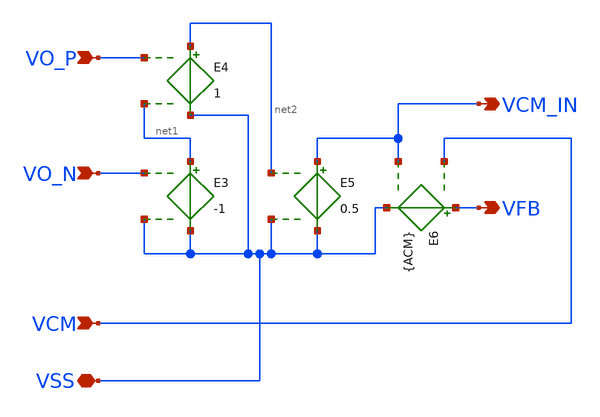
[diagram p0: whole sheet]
** sch_path: xschem/macro-models/cmfb_ideal.sch
**.subckt cmfb_ideal VO_P VO_N VCM VSS VFB VCM_IN
*.ipin VO_P
*.ipin VO_N
*.ipin VCM
*.iopin VSS
*.opin VFB
*.opin VCM_IN
E3 net1 VSS VO_N VSS -1
E4 net2 VSS VO_P net1 1
E5 VCM_IN VSS net2 VSS 0.5
E6 VFB VSS VCM VCM_IN {ACM}
**.ends
.end
